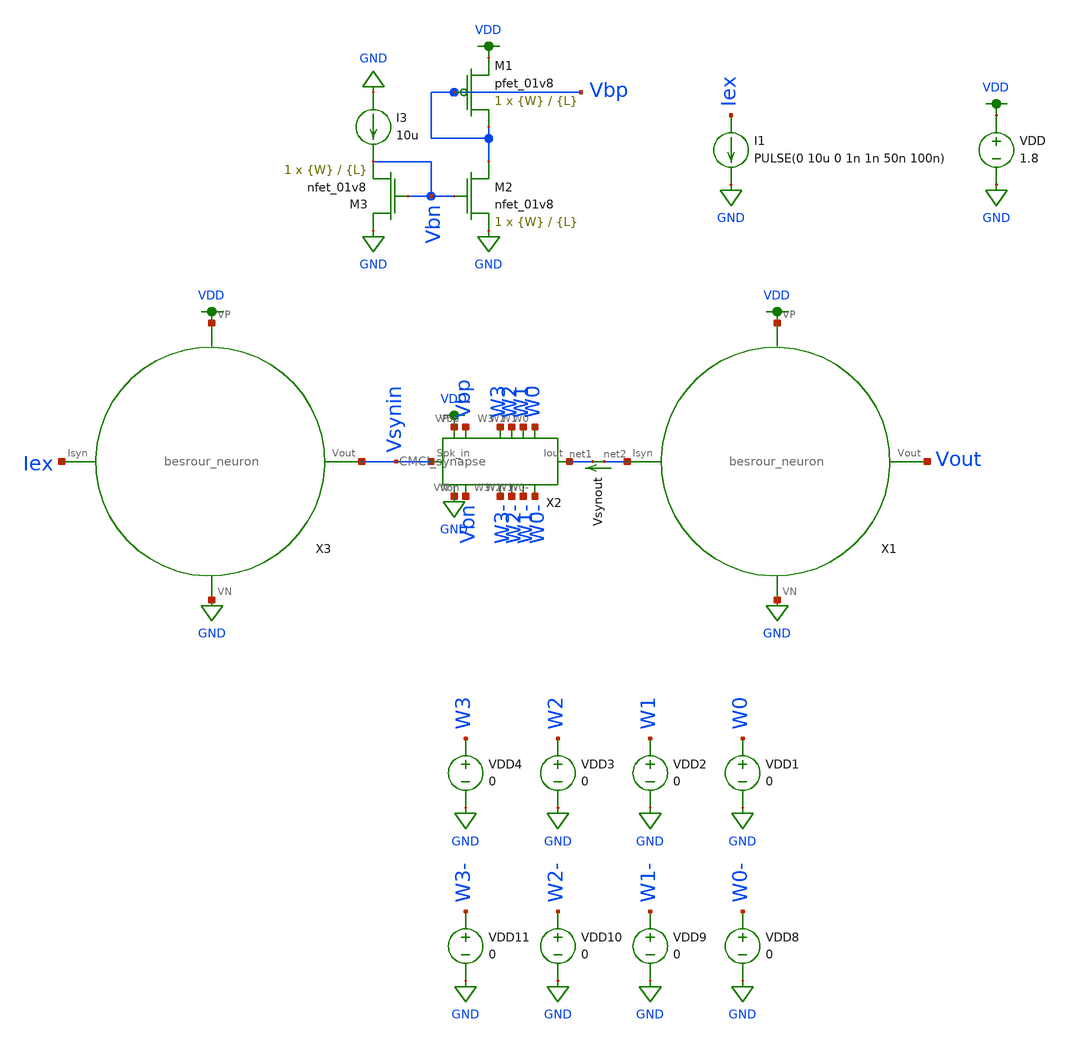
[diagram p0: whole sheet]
** sch_path: schematic/tran_besrour_neuron.sch
**.subckt tran_besrour_neuron
VDD VDD GND 1.8
X1 net2 Vout VDD GND besrour_neuron
X2 VDD Vbp W3 W2 W1 W0 net1 W0- W1- W2- W3- Vbn GND Vsynin CMCI_synapse
XM1 Vbp Vbp VDD VDD sky130_fd_pr__pfet_01v8 L={L} W={W} nf=1 ad='int((nf+1)/2) * W/nf * 0.29' as='int((nf+2)/2) * W/nf * 0.29'
+ pd='2*int((nf+1)/2) * (W/nf + 0.29)' ps='2*int((nf+2)/2) * (W/nf + 0.29)' nrd='0.29 / W' nrs='0.29 / W'
+ sa=0 sb=0 sd=0 mult=1 m=1
XM2 Vbp Vbn GND GND sky130_fd_pr__nfet_01v8 L={L} W={W} nf=1 ad='int((nf+1)/2) * W/nf * 0.29' as='int((nf+2)/2) * W/nf * 0.29'
+ pd='2*int((nf+1)/2) * (W/nf + 0.29)' ps='2*int((nf+2)/2) * (W/nf + 0.29)' nrd='0.29 / W' nrs='0.29 / W'
+ sa=0 sb=0 sd=0 mult=1 m=1
XM3 GND Vbn Vbn GND sky130_fd_pr__nfet_01v8 L={L} W={W} nf=1 ad='int((nf+1)/2) * W/nf * 0.29' as='int((nf+2)/2) * W/nf * 0.29'
+ pd='2*int((nf+1)/2) * (W/nf + 0.29)' ps='2*int((nf+2)/2) * (W/nf + 0.29)' nrd='0.29 / W' nrs='0.29 / W'
+ sa=0 sb=0 sd=0 mult=1 m=1
I3 GND Vbn 10u
VDD1 W0 GND 0
VDD2 W1 GND 0
VDD3 W2 GND 0
VDD4 W3 GND 0
VDD8 W0- GND 0
VDD9 W1- GND 0
VDD10 W2- GND 0
VDD11 W3- GND 0
Vsynout net2 net1 0
.save i(vsynout)
X3 Iex Vsynin VDD GND besrour_neuron
I1 Iex GND PULSE(0 10u 0 1n 1n 50n 100n)
**** begin user architecture code

.param W=1
.param L=0.15
.tran 0.1n 250n
.save Iex v(Vsynin) v(Vout)


.option wnflag=1
.param MC_SWITCH=0.0
.lib ~/skywater/skywater-pdk/libraries/sky130_fd_pr_ngspice/latest/models/sky130.lib.spice tt

**** end user architecture code
**.ends
.GLOBAL GND
.GLOBAL VDD
.end
